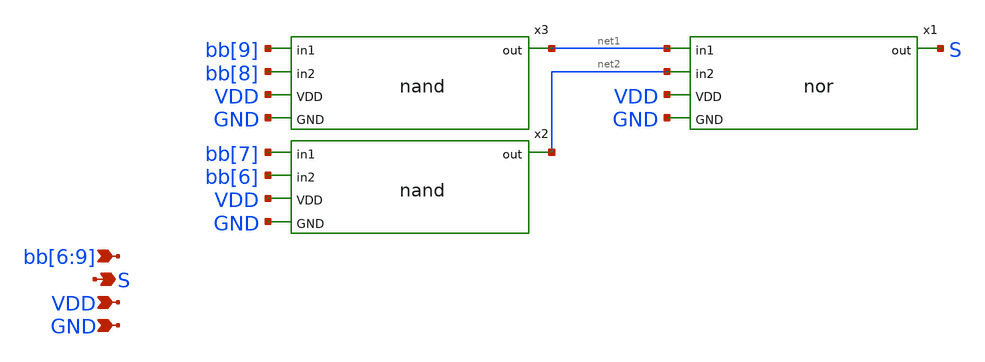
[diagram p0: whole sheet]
** sch_path: xschem/seg_selector_1_logic.sch
**.subckt seg_selector_1_logic S GND VDD bb[6],bb[7],bb[8],bb[9]
*.opin S
*.ipin GND
*.ipin VDD
*.ipin bb[6],bb[7],bb[8],bb[9]
x2 bb[7] bb[6] net2 VDD GND nand
x3 bb[9] bb[8] net1 VDD GND nand
x1 net1 net2 S VDD GND nor
**.ends

* expanding   symbol:  nand.sym # of pins=5
** sym_path: xschem/nand.sym
** sch_path: xschem/nand.sch
.subckt nand in1 in2 out VDD GND
*.ipin in2
*.opin out
*.ipin VDD
*.ipin GND
*.ipin in1
.param wp=0.63 wn=0.42 l=0.15
XM1 out in1 VDD VDD sky130_fd_pr__pfet_01v8 L=l W=wp nf=1 ad='int((nf+1)/2) * W/nf * 0.29' as='int((nf+2)/2) * W/nf * 0.29'
+ pd='2*int((nf+1)/2) * (W/nf + 0.29)' ps='2*int((nf+2)/2) * (W/nf + 0.29)' nrd='0.29 / W' nrs='0.29 / W'
+ sa=0 sb=0 sd=0 mult=1 m=1
XM2 out in2 VDD VDD sky130_fd_pr__pfet_01v8 L=l W=wp nf=1 ad='int((nf+1)/2) * W/nf * 0.29' as='int((nf+2)/2) * W/nf * 0.29'
+ pd='2*int((nf+1)/2) * (W/nf + 0.29)' ps='2*int((nf+2)/2) * (W/nf + 0.29)' nrd='0.29 / W' nrs='0.29 / W'
+ sa=0 sb=0 sd=0 mult=1 m=1
XM3 out in2 net1 GND sky130_fd_pr__nfet_01v8 L=l W=wn nf=1 ad='int((nf+1)/2) * W/nf * 0.29' as='int((nf+2)/2) * W/nf * 0.29'
+ pd='2*int((nf+1)/2) * (W/nf + 0.29)' ps='2*int((nf+2)/2) * (W/nf + 0.29)' nrd='0.29 / W' nrs='0.29 / W'
+ sa=0 sb=0 sd=0 mult=1 m=1
XM4 net1 in1 GND GND sky130_fd_pr__nfet_01v8 L=l W=wn nf=1 ad='int((nf+1)/2) * W/nf * 0.29' as='int((nf+2)/2) * W/nf * 0.29'
+ pd='2*int((nf+1)/2) * (W/nf + 0.29)' ps='2*int((nf+2)/2) * (W/nf + 0.29)' nrd='0.29 / W' nrs='0.29 / W'
+ sa=0 sb=0 sd=0 mult=1 m=1
.ends


* expanding   symbol:  nor.sym # of pins=5
** sym_path: xschem/nor.sym
** sch_path: xschem/nor.sch
.subckt nor in1 in2 out VDD GND
*.ipin in2
*.opin out
*.ipin VDD
*.ipin GND
*.ipin in1
.param wp=0.84 wn=0.42 l=0.15
XM1 out in2 net1 VDD sky130_fd_pr__pfet_01v8 L=l W=wp nf=1 ad='int((nf+1)/2) * W/nf * 0.29' as='int((nf+2)/2) * W/nf * 0.29'
+ pd='2*int((nf+1)/2) * (W/nf + 0.29)' ps='2*int((nf+2)/2) * (W/nf + 0.29)' nrd='0.29 / W' nrs='0.29 / W'
+ sa=0 sb=0 sd=0 mult=1 m=1
XM2 net1 in1 VDD VDD sky130_fd_pr__pfet_01v8 L=l W=wp nf=1 ad='int((nf+1)/2) * W/nf * 0.29' as='int((nf+2)/2) * W/nf * 0.29'
+ pd='2*int((nf+1)/2) * (W/nf + 0.29)' ps='2*int((nf+2)/2) * (W/nf + 0.29)' nrd='0.29 / W' nrs='0.29 / W'
+ sa=0 sb=0 sd=0 mult=1 m=1
XM3 out in2 GND GND sky130_fd_pr__nfet_01v8 L=l W=wn nf=1 ad='int((nf+1)/2) * W/nf * 0.29' as='int((nf+2)/2) * W/nf * 0.29'
+ pd='2*int((nf+1)/2) * (W/nf + 0.29)' ps='2*int((nf+2)/2) * (W/nf + 0.29)' nrd='0.29 / W' nrs='0.29 / W'
+ sa=0 sb=0 sd=0 mult=1 m=1
XM4 out in1 GND GND sky130_fd_pr__nfet_01v8 L=l W=wn nf=1 ad='int((nf+1)/2) * W/nf * 0.29' as='int((nf+2)/2) * W/nf * 0.29'
+ pd='2*int((nf+1)/2) * (W/nf + 0.29)' ps='2*int((nf+2)/2) * (W/nf + 0.29)' nrd='0.29 / W' nrs='0.29 / W'
+ sa=0 sb=0 sd=0 mult=1 m=1
.ends

.end
